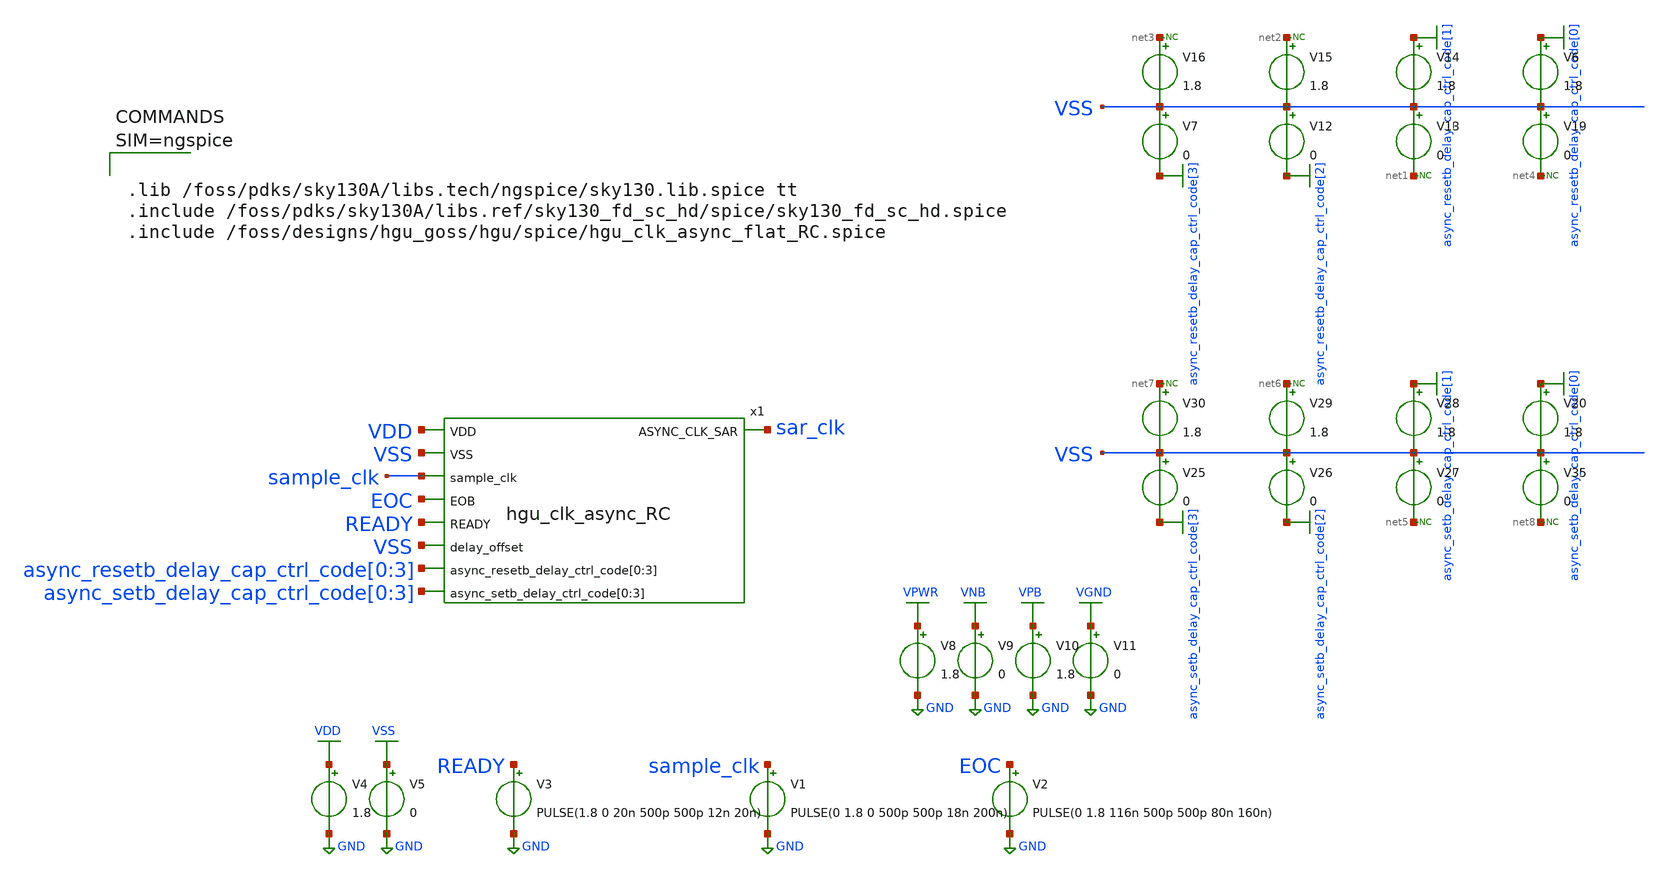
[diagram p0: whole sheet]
** sch_path: hgu/tb/tb_hgu_clk_async.sch
**.subckt tb_hgu_clk_async
V3 READY GND PULSE(1.8 0 20n 500p 500p 12n 20n)
x1 sar_clk VDD VSS sample_clk EOC READY VSS async_resetb_delay_cap_ctrl_code[0]
+ async_resetb_delay_cap_ctrl_code[1] async_resetb_delay_cap_ctrl_code[2] async_resetb_delay_cap_ctrl_code[3]
+ async_setb_delay_cap_ctrl_code[0] async_setb_delay_cap_ctrl_code[1] async_setb_delay_cap_ctrl_code[2]
+ async_setb_delay_cap_ctrl_code[3] hgu_clk_async_RC
V4 VDD GND 1.8
V5 VSS GND 0
V1 sample_clk GND PULSE(0 1.8 0 500p 500p 18n 200n)
V2 EOC GND PULSE(0 1.8 116n 500p 500p 80n 160n)
V8 VPWR GND 1.8
V9 VNB GND 0
V10 VPB GND 1.8
V11 VGND GND 0
V6 async_resetb_delay_cap_ctrl_code[0] VSS 1.8
V7 VSS async_resetb_delay_cap_ctrl_code[3] 0
V12 VSS async_resetb_delay_cap_ctrl_code[2] 0
V13 VSS net1 0
V14 async_resetb_delay_cap_ctrl_code[1] VSS 1.8
V15 net2 VSS 1.8
V16 net3 VSS 1.8
V19 VSS net4 0
* noconn #net3
* noconn #net2
* noconn #net1
* noconn #net4
V20 async_setb_delay_cap_ctrl_code[0] VSS 1.8
V25 VSS async_setb_delay_cap_ctrl_code[3] 0
V26 VSS async_setb_delay_cap_ctrl_code[2] 0
V27 VSS net5 0
V28 async_setb_delay_cap_ctrl_code[1] VSS 1.8
V29 net6 VSS 1.8
V30 net7 VSS 1.8
V35 VSS net8 0
* noconn #net7
* noconn #net6
* noconn #net5
* noconn #net8
**** begin user architecture code



.tran 40ps 150ns

.control
	option temp = 25
	let vdd_act = 1.8

	alter V1 vdd_act

	run
	plot V(READY)-2 V(sample_clk) V(EOC)+2 V(sar_clk)+4 V(sar_clk)-2 V(sar_clk)

        let l_vdd = vdd_act * 0.2
        let h_vdd = vdd_act * 0.8
        let m_vdd = vdd_act * 0.5
        meas tran rising_s find time when V(sar_clk)=l_vdd RISE=1 TD=10n
        meas tran rising_e find time when V(sar_clk)=h_vdd RISE=1 TD=10n
        let rising_time = rising_e-rising_s
        meas tran falling_s find time when V(sar_clk)=h_vdd FALL=1 TD=10n
        meas tran falling_e find time when V(sar_clk)=l_vdd FALL=1 TD=10n
        let falling_time = falling_e-falling_s
        meas tran IN find time when V(sample_clk)=m_vdd FALL=1 TD=10n
        meas tran OUT find time when V(sar_clk)=m_vdd RISE=1 TD=10n
        let rising_delay_1 = OUT-IN
        meas tran IN find time when V(ready)=m_vdd RISE=1 TD=24n
        meas tran OUT find time when V(sar_clk)=m_vdd RISE=1 TD=24n
        let rising_delay_2 = OUT-IN

	print rising_time falling_time rising_delay_1 rising_delay_2

 .endc
.save all






.lib /foss/pdks/sky130A/libs.tech/ngspice/sky130.lib.spice tt
.include /foss/pdks/sky130A/libs.ref/sky130_fd_sc_hd/spice/sky130_fd_sc_hd.spice
.include /foss/designs/hgu_goss/hgu/spice/hgu_clk_async_flat_RC.spice



**** end user architecture code
**.ends
.GLOBAL GND
.GLOBAL VDD
.GLOBAL VSS
.GLOBAL VGND
.GLOBAL VNB
.GLOBAL VPB
.GLOBAL VPWR
.GLOBAL async_resetb_delay_cap_ctrl_code[3]
.GLOBAL async_resetb_delay_cap_ctrl_code[2]
.GLOBAL async_resetb_delay_cap_ctrl_code[1]
.GLOBAL async_resetb_delay_cap_ctrl_code[0]
.GLOBAL async_setb_delay_cap_ctrl_code[3]
.GLOBAL async_setb_delay_cap_ctrl_code[2]
.GLOBAL async_setb_delay_cap_ctrl_code[1]
.GLOBAL async_setb_delay_cap_ctrl_code[0]
.end
